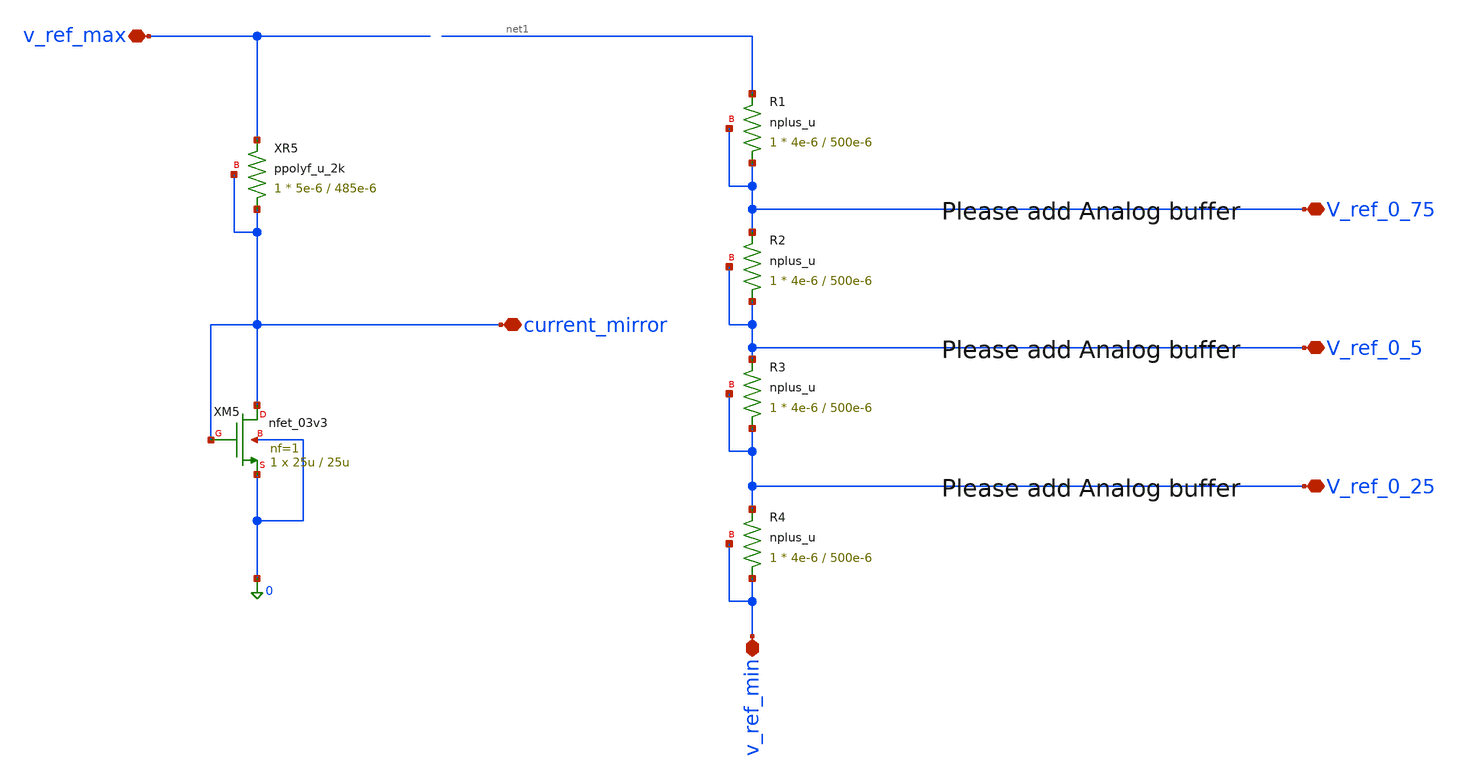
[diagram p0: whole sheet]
** sch_path: Felix/Reference_circuits_v2.sch
**.subckt Reference_circuits_v2 v_ref_max v_ref_min current_mirror V_ref_0_75 V_ref_0_5 V_ref_0_25
*.iopin v_ref_max
*.iopin v_ref_min
*.iopin current_mirror
*.iopin V_ref_0_75
*.iopin V_ref_0_5
*.iopin V_ref_0_25
XR1 V_ref_0_75 net1 V_ref_0_75 nplus_u r_width=4e-6 r_length=500e-6 m=1
XR2 V_ref_0_5 V_ref_0_75 V_ref_0_5 nplus_u r_width=4e-6 r_length=500e-6 m=1
XR3 V_ref_0_25 V_ref_0_5 V_ref_0_25 nplus_u r_width=4e-6 r_length=500e-6 m=1
XR4 v_ref_min V_ref_0_25 v_ref_min nplus_u r_width=4e-6 r_length=500e-6 m=1
XM5 current_mirror current_mirror 0 0 nfet_03v3 L=25u W=25u nf=1 ad='int((nf+1)/2) * W/nf * 0.18u' as='int((nf+2)/2) * W/nf * 0.18u'
+ pd='2*int((nf+1)/2) * (W/nf + 0.18u)' ps='2*int((nf+2)/2) * (W/nf + 0.18u)' nrd='0.18u / W' nrs='0.18u / W'
+ sa=0 sb=0 sd=0 m=1
XR5 current_mirror v_ref_max current_mirror ppolyf_u_2k r_width=5e-6 r_length=485e-6 m=1
**.ends
.end
